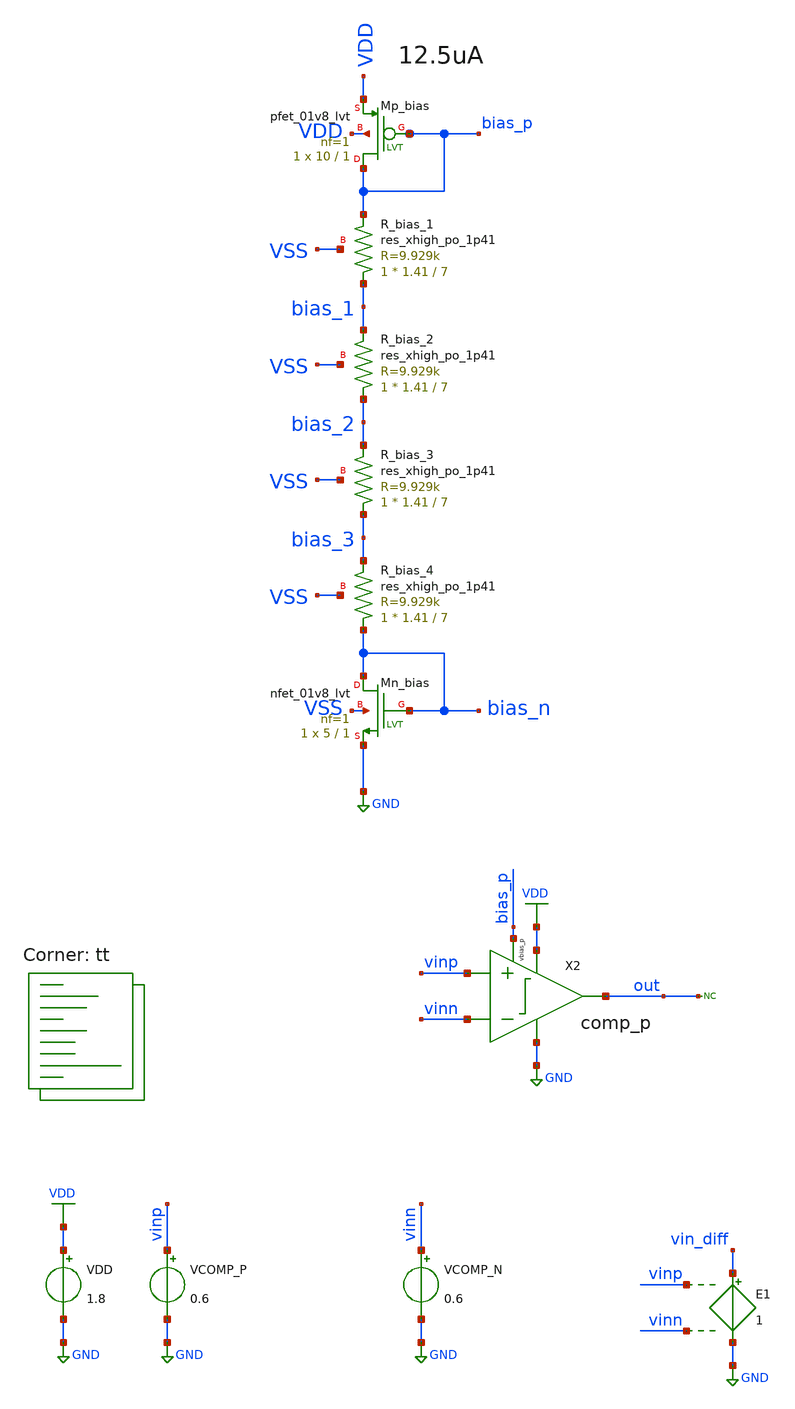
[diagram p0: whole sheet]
** sch_path: xsch/tb/comp_p/tb_comp_p_dc_sweep.sch
**.subckt tb_comp_p_dc_sweep
VDD VDD GND 1.8
* noconn out
VCOMP_N vinn GND 0.6
XR_bias_1 bias_1 bias_p VSS sky130_fd_pr__res_xhigh_po_1p41 L=7 mult=1 m=1
XMn_bias bias_n bias_n GND VSS sky130_fd_pr__nfet_01v8_lvt L=1 W=5 nf=1 ad='int((nf+1)/2) * W/nf * 0.29'
+ as='int((nf+2)/2) * W/nf * 0.29' pd='2*int((nf+1)/2) * (W/nf + 0.29)' ps='2*int((nf+2)/2) * (W/nf + 0.29)'
+ nrd='0.29 / W' nrs='0.29 / W' sa=0 sb=0 sd=0 mult=1 m=1
XMp_bias bias_p bias_p VDD VDD sky130_fd_pr__pfet_01v8_lvt L=1 W=10 nf=1 ad='int((nf+1)/2) * W/nf * 0.29'
+ as='int((nf+2)/2) * W/nf * 0.29' pd='2*int((nf+1)/2) * (W/nf + 0.29)' ps='2*int((nf+2)/2) * (W/nf + 0.29)'
+ nrd='0.29 / W' nrs='0.29 / W' sa=0 sb=0 sd=0 mult=1 m=1
XR_bias_2 bias_2 bias_1 VSS sky130_fd_pr__res_xhigh_po_1p41 L=7 mult=1 m=1
XR_bias_3 bias_3 bias_2 VSS sky130_fd_pr__res_xhigh_po_1p41 L=7 mult=1 m=1
XR_bias_4 bias_n bias_3 VSS sky130_fd_pr__res_xhigh_po_1p41 L=7 mult=1 m=1
VCOMP_P vinp GND 0.6
E1 vin_diff GND vinp vinn 1
X2 vinp vinn bias_p out VDD GND comp_p
**** begin user architecture code



* control language script

.control
;tran 100p 500n               ; simulation command 1

set xbrushwidth=2
;plot v(in) v(out)

;write $inputdir/outtran.out v(in) v(out)

;reset

let v_TL = vector(1)
let v_TH = vector(2)

dc VCOMP_N 0 1.2 0.01e-3              ; simulation command 2

plot v(out) v(vin_diff) xlabel 'V_TL measurement'              ; v(in) not required because it is the
+ x axis already

meas dc vrampval find v(vin_diff) when v(out)=0.9
let vgain = vecmin(deriv(v(out)))
let v_TL = vrampval

echo ---- My Measurements ----
echo Voffset:  $&vrampval
echo Maximum Gain: $&vgain
echo -------------------------


dc VCOMP_P 0 1.2 0.01e-3              ; simulation command 2

plot v(out) v(vin_diff) xlabel 'V_TH measurement'       ;

meas dc vrampval find v(vin_diff) when v(out)=0.9
let vgain = vecmax(deriv(v(out)))
let v_TH = vrampval

echo ---- My Measurements ----
echo Voffset:  $&vrampval
echo Maximum Gain: $&vgain
echo -------------------------

reset

echo V_tl $&v_TL
echo V_th $&v_TH
let v_hyst = mag($&v_TL - $&v_TH)
echo V_hyst $&v_hyst
let voffset = -$&v_hyst/2.0
echo V_offset $&voffset

rusage

.endc
.end



.lib $::SKYWATER_MODELS/sky130.lib.spice tt
**** end user architecture code
**.ends

* expanding   symbol:  /home/bmott/ttsky25b_tiny_chaos/xsch/ip/comparators/comp_p/comp_p.sym # of
*+ pins=6
** sym_path: /home/bmott/ttsky25b_tiny_chaos/xsch/ip/comparators/comp_p/comp_p.sym
** sch_path: /home/bmott/ttsky25b_tiny_chaos/xsch/ip/comparators/comp_p/comp_p.sch
.subckt comp_p vinp vinn vbias_p vout vdd vss
*.iopin vdd
*.iopin vss
*.ipin vbias_p
*.ipin vinn
*.ipin vinp
*.opin vout
XMp_inn1 latch_left vinn tail vdd sky130_fd_pr__pfet_01v8_lvt L=0.35 W=10 nf=1 ad='int((nf+1)/2) * W/nf * 0.29'
+ as='int((nf+2)/2) * W/nf * 0.29' pd='2*int((nf+1)/2) * (W/nf + 0.29)' ps='2*int((nf+2)/2) * (W/nf + 0.29)'
+ nrd='0.29 / W' nrs='0.29 / W' sa=0 sb=0 sd=0 mult=4 m=4
XMp_inp1 latch_right vinp tail vdd sky130_fd_pr__pfet_01v8_lvt L=0.35 W=10 nf=1 ad='int((nf+1)/2) * W/nf * 0.29'
+ as='int((nf+2)/2) * W/nf * 0.29' pd='2*int((nf+1)/2) * (W/nf + 0.29)' ps='2*int((nf+2)/2) * (W/nf + 0.29)'
+ nrd='0.29 / W' nrs='0.29 / W' sa=0 sb=0 sd=0 mult=4 m=4
XMn_diode_left1 latch_left latch_left vss vss sky130_fd_pr__nfet_01v8_lvt L=1 W=4 nf=1 ad='int((nf+1)/2) * W/nf * 0.29'
+ as='int((nf+2)/2) * W/nf * 0.29' pd='2*int((nf+1)/2) * (W/nf + 0.29)' ps='2*int((nf+2)/2) * (W/nf + 0.29)'
+ nrd='0.29 / W' nrs='0.29 / W' sa=0 sb=0 sd=0 mult=1 m=1
XMn_cs_left latch_right latch_left vss vss sky130_fd_pr__nfet_01v8_lvt L=1 W=5 nf=1 ad='int((nf+1)/2) * W/nf * 0.29'
+ as='int((nf+2)/2) * W/nf * 0.29' pd='2*int((nf+1)/2) * (W/nf + 0.29)' ps='2*int((nf+2)/2) * (W/nf + 0.29)'
+ nrd='0.29 / W' nrs='0.29 / W' sa=0 sb=0 sd=0 mult=1 m=1
XMn_diode_right latch_right latch_right vss vss sky130_fd_pr__nfet_01v8_lvt L=1 W=4 nf=1 ad='int((nf+1)/2) * W/nf * 0.29'
+ as='int((nf+2)/2) * W/nf * 0.29' pd='2*int((nf+1)/2) * (W/nf + 0.29)' ps='2*int((nf+2)/2) * (W/nf + 0.29)'
+ nrd='0.29 / W' nrs='0.29 / W' sa=0 sb=0 sd=0 mult=1 m=1
XMn_cs_right1 latch_left latch_right vss vss sky130_fd_pr__nfet_01v8_lvt L=1 W=5 nf=1 ad='int((nf+1)/2) * W/nf * 0.29'
+ as='int((nf+2)/2) * W/nf * 0.29' pd='2*int((nf+1)/2) * (W/nf + 0.29)' ps='2*int((nf+2)/2) * (W/nf + 0.29)'
+ nrd='0.29 / W' nrs='0.29 / W' sa=0 sb=0 sd=0 mult=1 m=1
XMp_tail tail vbias_p vdd vdd sky130_fd_pr__pfet_01v8_lvt L=1 W=10 nf=1 ad='int((nf+1)/2) * W/nf * 0.29'
+ as='int((nf+2)/2) * W/nf * 0.29' pd='2*int((nf+1)/2) * (W/nf + 0.29)' ps='2*int((nf+2)/2) * (W/nf + 0.29)'
+ nrd='0.29 / W' nrs='0.29 / W' sa=0 sb=0 sd=0 mult=1 m=1
XMn_out_right vout latch_right vss vss sky130_fd_pr__nfet_01v8_lvt L=1 W=5 nf=1 ad='int((nf+1)/2) * W/nf * 0.29'
+ as='int((nf+2)/2) * W/nf * 0.29' pd='2*int((nf+1)/2) * (W/nf + 0.29)' ps='2*int((nf+2)/2) * (W/nf + 0.29)'
+ nrd='0.29 / W' nrs='0.29 / W' sa=0 sb=0 sd=0 mult=1 m=1
XMn_out_left out_left latch_left vss vss sky130_fd_pr__nfet_01v8_lvt L=1 W=5 nf=1 ad='int((nf+1)/2) * W/nf * 0.29'
+ as='int((nf+2)/2) * W/nf * 0.29' pd='2*int((nf+1)/2) * (W/nf + 0.29)' ps='2*int((nf+2)/2) * (W/nf + 0.29)'
+ nrd='0.29 / W' nrs='0.29 / W' sa=0 sb=0 sd=0 mult=1 m=1
XMp_diode_left1 out_left out_left vdd vdd sky130_fd_pr__pfet_01v8_lvt L=1 W=8 nf=1 ad='int((nf+1)/2) * W/nf * 0.29'
+ as='int((nf+2)/2) * W/nf * 0.29' pd='2*int((nf+1)/2) * (W/nf + 0.29)' ps='2*int((nf+2)/2) * (W/nf + 0.29)'
+ nrd='0.29 / W' nrs='0.29 / W' sa=0 sb=0 sd=0 mult=1 m=1
XMp_out vout out_left vdd vdd sky130_fd_pr__pfet_01v8_lvt L=1 W=8 nf=1 ad='int((nf+1)/2) * W/nf * 0.29'
+ as='int((nf+2)/2) * W/nf * 0.29' pd='2*int((nf+1)/2) * (W/nf + 0.29)' ps='2*int((nf+2)/2) * (W/nf + 0.29)'
+ nrd='0.29 / W' nrs='0.29 / W' sa=0 sb=0 sd=0 mult=1 m=1
.ends

.GLOBAL VDD
.GLOBAL GND
.end
